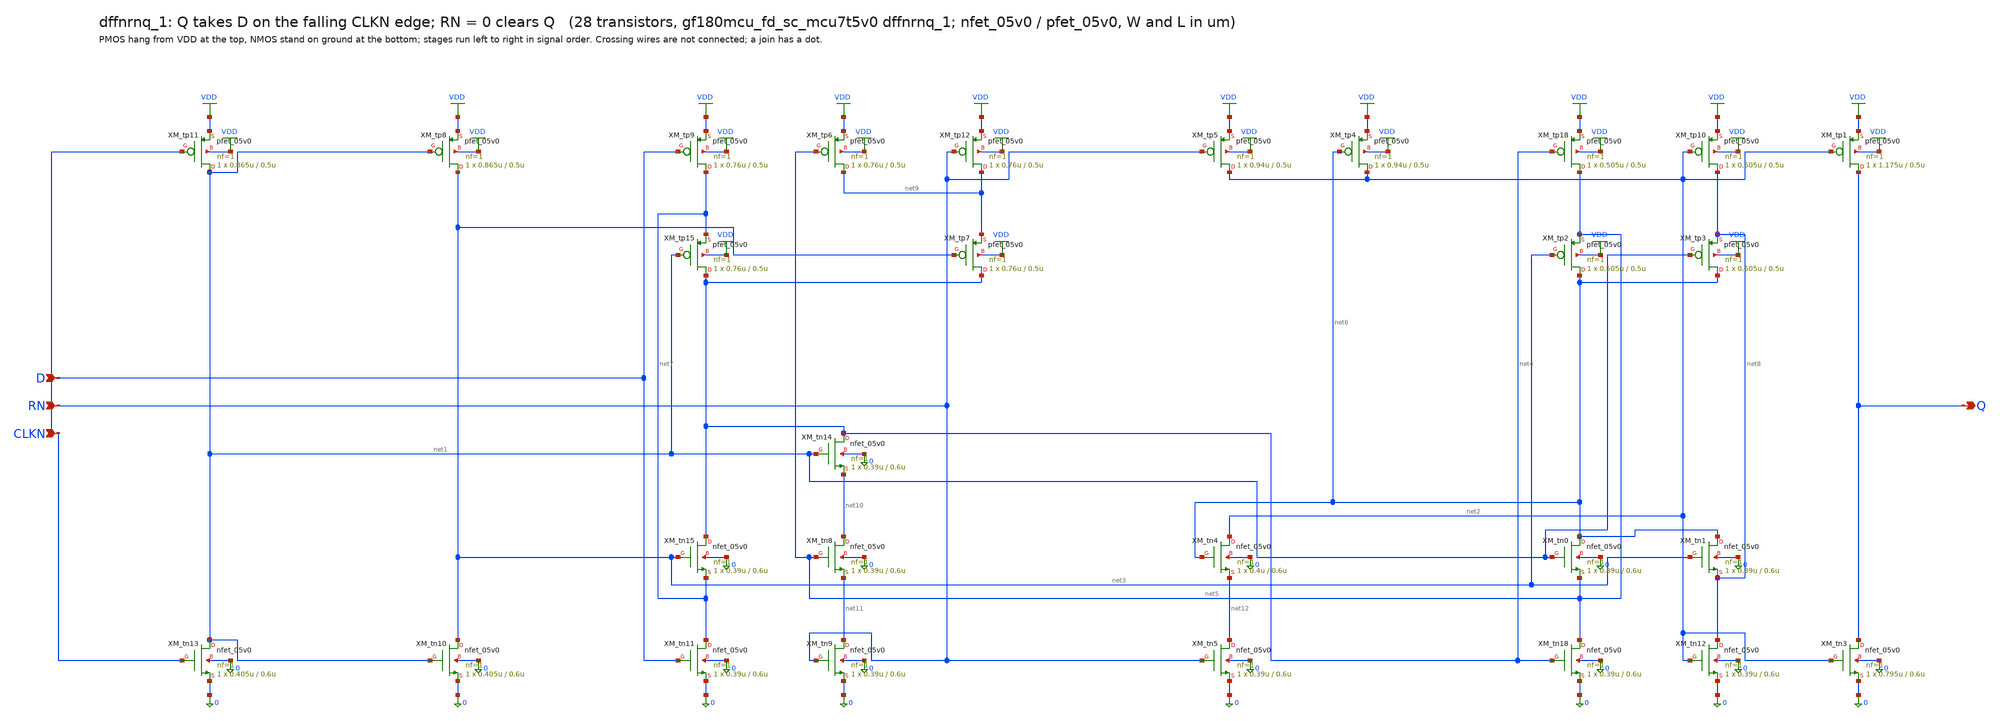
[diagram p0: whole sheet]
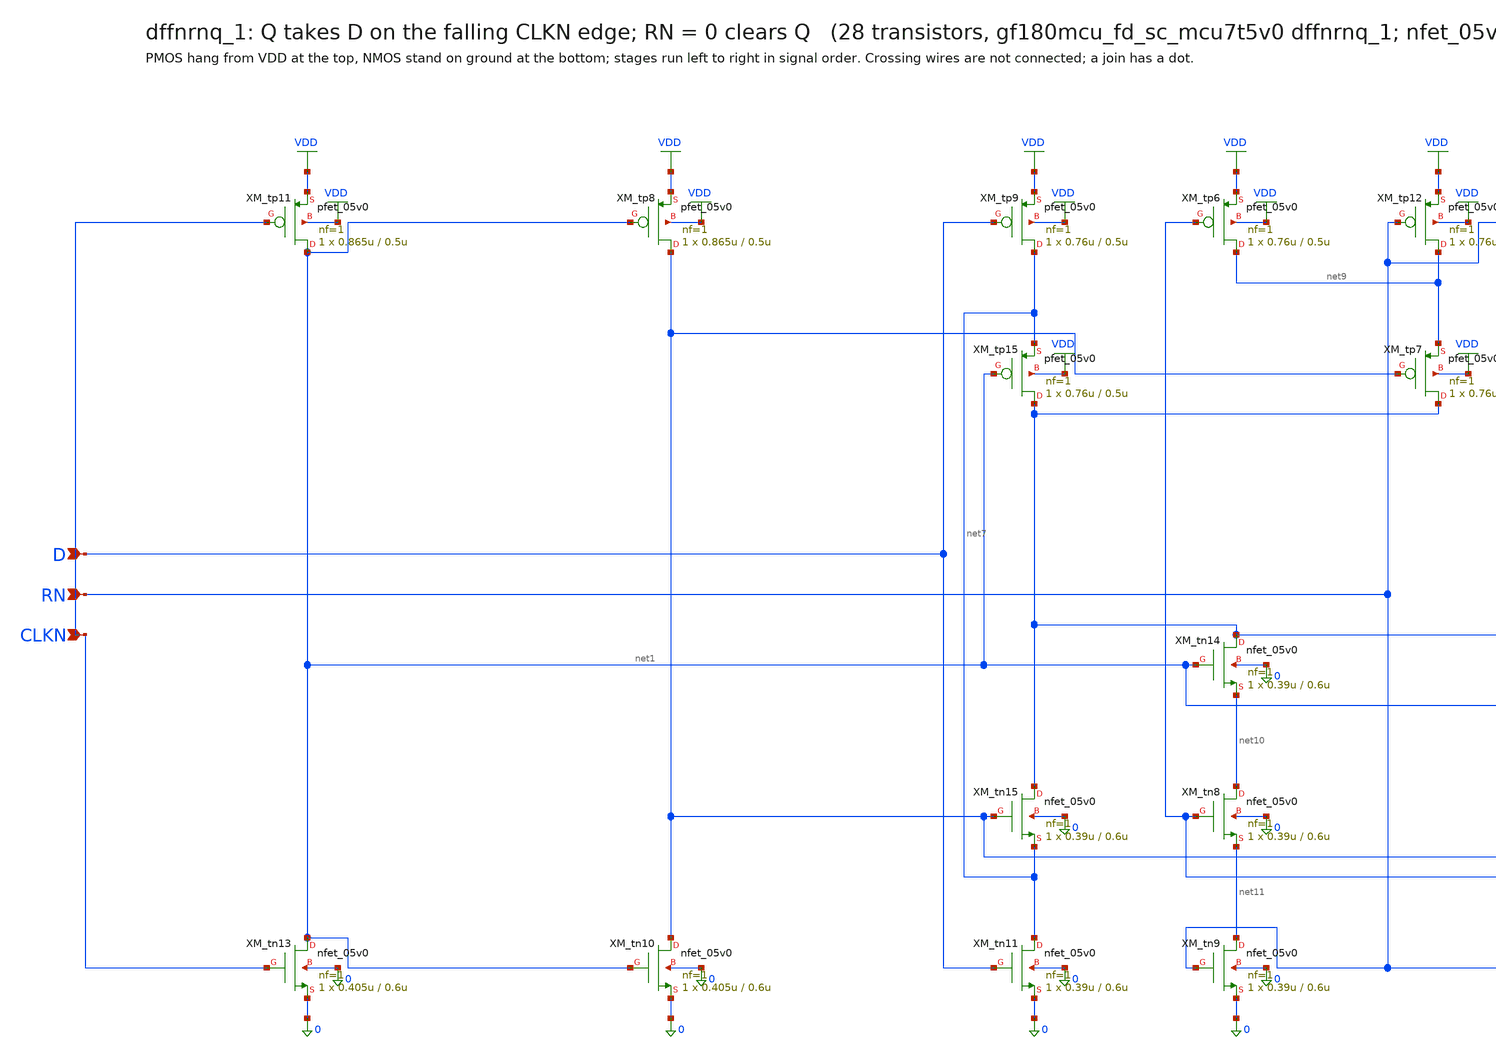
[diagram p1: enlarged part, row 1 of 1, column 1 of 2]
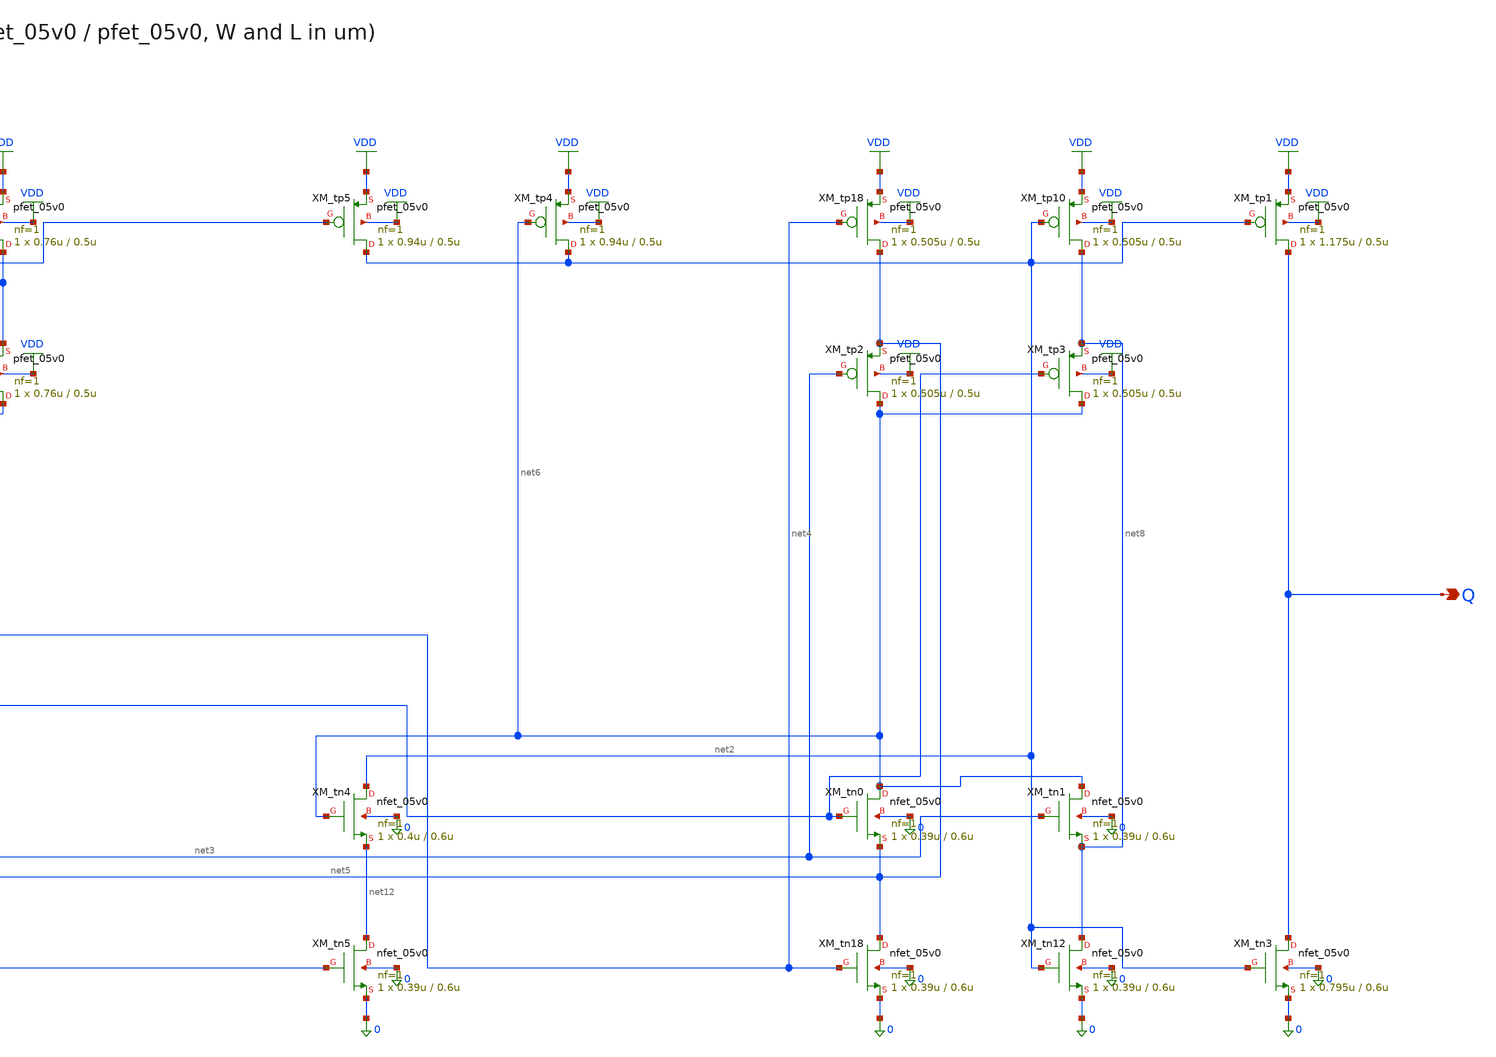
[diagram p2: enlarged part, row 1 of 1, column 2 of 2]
** sch_path: xschem/cells_tx/dffnrnq_1.sch
**.subckt dffnrnq_1 D RN CLKN Q
*.ipin D
*.ipin RN
*.ipin CLKN
*.opin Q
XM_tn13 net1 CLKN 0 0 nfet_05v0 L=0.6u W=0.405u nf=1 ad=2.025e-13 as=2.025e-13 pd=1.81e-06
+ ps=1.81e-06 nrd=0 nrs=0 sa=0 sb=0 sd=0 m=1
XM_tn10 net3 net1 0 0 nfet_05v0 L=0.6u W=0.405u nf=1 ad=2.025e-13 as=2.025e-13 pd=1.81e-06
+ ps=1.81e-06 nrd=0 nrs=0 sa=0 sb=0 sd=0 m=1
XM_tn11 net7 D 0 0 nfet_05v0 L=0.6u W=0.39u nf=1 ad=1.95e-13 as=1.95e-13 pd=1.78e-06 ps=1.78e-06
+ nrd=0 nrs=0 sa=0 sb=0 sd=0 m=1
XM_tn15 net4 net3 net7 0 nfet_05v0 L=0.6u W=0.39u nf=1 ad=1.95e-13 as=1.95e-13 pd=1.78e-06
+ ps=1.78e-06 nrd=0 nrs=0 sa=0 sb=0 sd=0 m=1
XM_tn14 net4 net1 net10 0 nfet_05v0 L=0.6u W=0.39u nf=1 ad=1.95e-13 as=1.95e-13 pd=1.78e-06
+ ps=1.78e-06 nrd=0 nrs=0 sa=0 sb=0 sd=0 m=1
XM_tn8 net10 net5 net11 0 nfet_05v0 L=0.6u W=0.39u nf=1 ad=1.95e-13 as=1.95e-13 pd=1.78e-06
+ ps=1.78e-06 nrd=0 nrs=0 sa=0 sb=0 sd=0 m=1
XM_tn9 net11 RN 0 0 nfet_05v0 L=0.6u W=0.39u nf=1 ad=1.95e-13 as=1.95e-13 pd=1.78e-06 ps=1.78e-06
+ nrd=0 nrs=0 sa=0 sb=0 sd=0 m=1
XM_tn18 net5 net4 0 0 nfet_05v0 L=0.6u W=0.39u nf=1 ad=1.95e-13 as=1.95e-13 pd=1.78e-06 ps=1.78e-06
+ nrd=0 nrs=0 sa=0 sb=0 sd=0 m=1
XM_tn0 net6 net1 net5 0 nfet_05v0 L=0.6u W=0.39u nf=1 ad=1.95e-13 as=1.95e-13 pd=1.78e-06
+ ps=1.78e-06 nrd=0 nrs=0 sa=0 sb=0 sd=0 m=1
XM_tn1 net6 net3 net8 0 nfet_05v0 L=0.6u W=0.39u nf=1 ad=1.95e-13 as=1.95e-13 pd=1.78e-06
+ ps=1.78e-06 nrd=0 nrs=0 sa=0 sb=0 sd=0 m=1
XM_tn12 net8 net2 0 0 nfet_05v0 L=0.6u W=0.39u nf=1 ad=1.95e-13 as=1.95e-13 pd=1.78e-06 ps=1.78e-06
+ nrd=0 nrs=0 sa=0 sb=0 sd=0 m=1
XM_tn5 net12 RN 0 0 nfet_05v0 L=0.6u W=0.39u nf=1 ad=1.95e-13 as=1.95e-13 pd=1.78e-06 ps=1.78e-06
+ nrd=0 nrs=0 sa=0 sb=0 sd=0 m=1
XM_tn4 net2 net6 net12 0 nfet_05v0 L=0.6u W=0.4u nf=1 ad=2e-13 as=2e-13 pd=1.8e-06 ps=1.8e-06 nrd=0
+ nrs=0 sa=0 sb=0 sd=0 m=1
XM_tn3 Q net2 0 0 nfet_05v0 L=0.6u W=0.795u nf=1 ad=3.975e-13 as=3.975e-13 pd=2.59e-06 ps=2.59e-06
+ nrd=0 nrs=0 sa=0 sb=0 sd=0 m=1
XM_tp11 net1 CLKN VDD VDD pfet_05v0 L=0.5u W=0.865u nf=1 ad=4.325e-13 as=4.325e-13 pd=2.73e-06
+ ps=2.73e-06 nrd=0 nrs=0 sa=0 sb=0 sd=0 m=1
XM_tp8 net3 net1 VDD VDD pfet_05v0 L=0.5u W=0.865u nf=1 ad=4.325e-13 as=4.325e-13 pd=2.73e-06
+ ps=2.73e-06 nrd=0 nrs=0 sa=0 sb=0 sd=0 m=1
XM_tp9 net7 D VDD VDD pfet_05v0 L=0.5u W=0.76u nf=1 ad=3.8e-13 as=3.8e-13 pd=2.52e-06 ps=2.52e-06
+ nrd=0 nrs=0 sa=0 sb=0 sd=0 m=1
XM_tp15 net4 net1 net7 VDD pfet_05v0 L=0.5u W=0.76u nf=1 ad=3.8e-13 as=3.8e-13 pd=2.52e-06
+ ps=2.52e-06 nrd=0 nrs=0 sa=0 sb=0 sd=0 m=1
XM_tp7 net4 net3 net9 VDD pfet_05v0 L=0.5u W=0.76u nf=1 ad=3.8e-13 as=3.8e-13 pd=2.52e-06
+ ps=2.52e-06 nrd=0 nrs=0 sa=0 sb=0 sd=0 m=1
XM_tp6 net9 net5 VDD VDD pfet_05v0 L=0.5u W=0.76u nf=1 ad=3.8e-13 as=3.8e-13 pd=2.52e-06 ps=2.52e-06
+ nrd=0 nrs=0 sa=0 sb=0 sd=0 m=1
XM_tp12 net9 RN VDD VDD pfet_05v0 L=0.5u W=0.76u nf=1 ad=3.8e-13 as=3.8e-13 pd=2.52e-06 ps=2.52e-06
+ nrd=0 nrs=0 sa=0 sb=0 sd=0 m=1
XM_tp18 net5 net4 VDD VDD pfet_05v0 L=0.5u W=0.505u nf=1 ad=2.525e-13 as=2.525e-13 pd=2.01e-06
+ ps=2.01e-06 nrd=0 nrs=0 sa=0 sb=0 sd=0 m=1
XM_tp2 net6 net3 net5 VDD pfet_05v0 L=0.5u W=0.505u nf=1 ad=2.525e-13 as=2.525e-13 pd=2.01e-06
+ ps=2.01e-06 nrd=0 nrs=0 sa=0 sb=0 sd=0 m=1
XM_tp3 net6 net1 net8 VDD pfet_05v0 L=0.5u W=0.505u nf=1 ad=2.525e-13 as=2.525e-13 pd=2.01e-06
+ ps=2.01e-06 nrd=0 nrs=0 sa=0 sb=0 sd=0 m=1
XM_tp10 net8 net2 VDD VDD pfet_05v0 L=0.5u W=0.505u nf=1 ad=2.525e-13 as=2.525e-13 pd=2.01e-06
+ ps=2.01e-06 nrd=0 nrs=0 sa=0 sb=0 sd=0 m=1
XM_tp5 net2 RN VDD VDD pfet_05v0 L=0.5u W=0.94u nf=1 ad=4.7e-13 as=4.7e-13 pd=2.88e-06 ps=2.88e-06
+ nrd=0 nrs=0 sa=0 sb=0 sd=0 m=1
XM_tp4 net2 net6 VDD VDD pfet_05v0 L=0.5u W=0.94u nf=1 ad=4.7e-13 as=4.7e-13 pd=2.88e-06 ps=2.88e-06
+ nrd=0 nrs=0 sa=0 sb=0 sd=0 m=1
XM_tp1 Q net2 VDD VDD pfet_05v0 L=0.5u W=1.175u nf=1 ad=5.875e-13 as=5.875e-13 pd=3.35e-06
+ ps=3.35e-06 nrd=0 nrs=0 sa=0 sb=0 sd=0 m=1
**.ends
.GLOBAL VDD
.end
